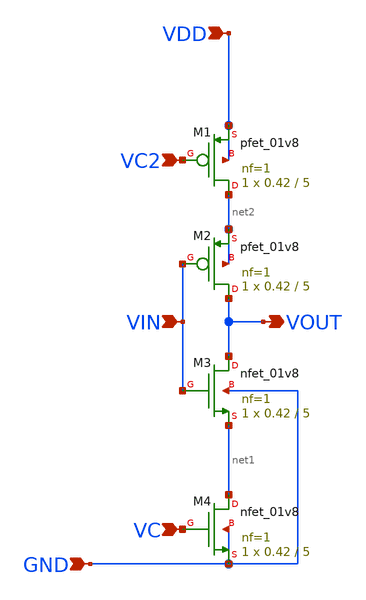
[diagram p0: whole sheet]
** sch_path: design/LELO_SVOD_SKY130A/LELO_RING_DEL_VC.sch
**.subckt LELO_RING_DEL_VC VIN VDD GND VOUT VC VC2
*.ipin VIN
*.ipin VDD
*.ipin GND
*.opin VOUT
*.ipin VC
*.ipin VC2
XM1 net2 VC2 VDD VDD sky130_fd_pr__pfet_01v8 L=5 W=0.42 nf=1 ad='int((1 + 1)/2) * 0.42 / 1 * 0.29' as='int((1 + 2)/2) * 0.42 / 1 * 0.29'
+ pd='2*int((1 + 1)/2) * (0.42 / 1 + 0.29)' ps='2*int((1 + 2)/2) * (0.42 / 1 + 0.29)' nrd='0.29 / 0.42 '
+ nrs='0.29 / 0.42 ' sa=0 sb=0 sd=0 mult=1 m=1
XM2 VOUT VIN net2 net2 sky130_fd_pr__pfet_01v8 L=5 W=0.42 nf=1 ad='int((1 + 1)/2) * 0.42 / 1 * 0.29'
+ as='int((1 + 2)/2) * 0.42 / 1 * 0.29' pd='2*int((1 + 1)/2) * (0.42 / 1 + 0.29)' ps='2*int((1 + 2)/2) * (0.42 / 1 + 0.29)'
+ nrd='0.29 / 0.42 ' nrs='0.29 / 0.42 ' sa=0 sb=0 sd=0 mult=1 m=1
XM3 VOUT VIN net1 GND sky130_fd_pr__nfet_01v8 L=5 W=0.42 nf=1 ad='int((1 + 1)/2) * 0.42 / 1 * 0.29' as='int((1 + 2)/2) * 0.42 / 1 * 0.29'
+ pd='2*int((1 + 1)/2) * (0.42 / 1 + 0.29)' ps='2*int((1 + 2)/2) * (0.42 / 1 + 0.29)' nrd='0.29 / 0.42 '
+ nrs='0.29 / 0.42 ' sa=0 sb=0 sd=0 mult=1 m=1
XM4 net1 VC GND GND sky130_fd_pr__nfet_01v8 L=5 W=0.42 nf=1 ad='int((1 + 1)/2) * 0.42 / 1 * 0.29' as='int((1 + 2)/2) * 0.42 / 1 * 0.29'
+ pd='2*int((1 + 1)/2) * (0.42 / 1 + 0.29)' ps='2*int((1 + 2)/2) * (0.42 / 1 + 0.29)' nrd='0.29 / 0.42 '
+ nrs='0.29 / 0.42 ' sa=0 sb=0 sd=0 mult=1 m=1
**.ends
.end
